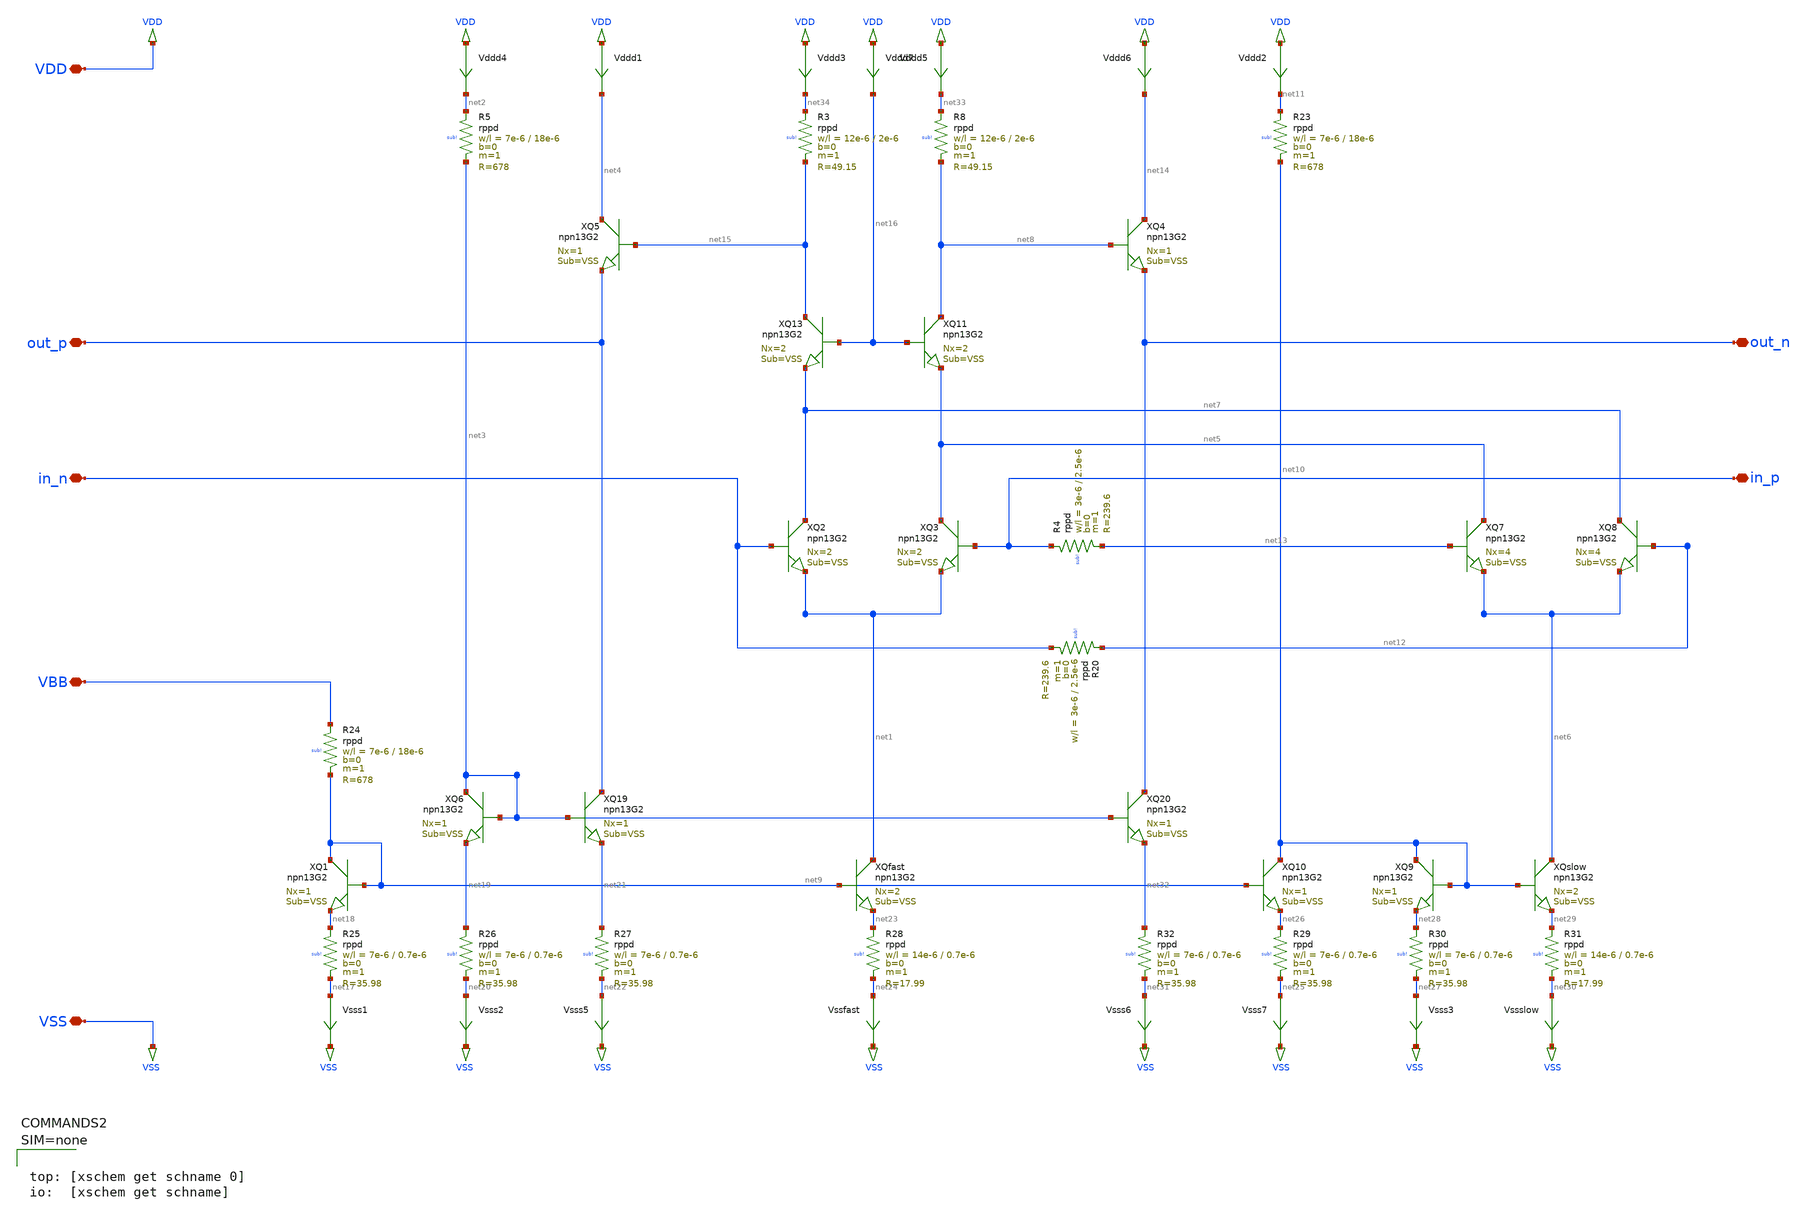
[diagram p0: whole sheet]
** sch_path: HBT_VCO_active_L/design_data/xschem/VCO_HBT_inv_dual_dly.sch
* Copyright (C) 1998-2023 Stefan Frederik Schippers
* This program is free software; you can redistribute it and/or modify
* it under the terms of the GNU General Public License as published by
* the Free Software Foundation; either version 2 of the License, or
* (at your option) any later version.
* This program is distributed in the hope that it will be useful,
* but WITHOUT ANY WARRANTY; without even the implied warranty of
* MERCHANTABILITY or FITNESS FOR A PARTICULAR PURPOSE.  See the
* GNU General Public License for more details.
* You should have received a copy of the GNU General Public License
* along with this program; if not, write to the Free Software
**.subckt VCO_HBT_inv_dual_dly VSS VBB out_p out_n VDD in_n in_p
*.iopin VSS
*.iopin VBB
*.iopin out_p
*.iopin out_n
*.iopin VDD
*.iopin in_n
*.iopin in_p
Vssfast net24 VSS 0
.save i(vssfast)
XQfast net1 net9 net23 VSS npn13G2 Nx=2
Vsss5 net22 VSS 0
.save i(vsss5)
XQ19 out_p net3 net21 VSS npn13G2 Nx=1
Vsss6 net31 VSS 0
.save i(vsss6)
XQ20 out_n net3 net32 VSS npn13G2 Nx=1
XQ2 net7 in_n net1 VSS npn13G2 Nx=2
XQ3 net5 in_p net1 VSS npn13G2 Nx=2
XQ4 net14 net8 out_n VSS npn13G2 Nx=1
XQ5 net4 net15 out_p VSS npn13G2 Nx=1
Vsss2 net20 VSS 0
.save i(vsss2)
XQ6 net3 net3 net19 VSS npn13G2 Nx=1
Vddd4 VDD net2 0
.save i(vddd4)
Vddd3 VDD net34 0
.save i(vddd3)
Vddd1 VDD net4 0
.save i(vddd1)
Vddd5 VDD net33 0
.save i(vddd5)
Vddd6 VDD net14 0
.save i(vddd6)
Vssslow net30 VSS 0
.save i(vssslow)
XQslow net6 net10 net29 VSS npn13G2 Nx=2
XQ7 net5 net13 net6 VSS npn13G2 Nx=4
XQ8 net7 net12 net6 VSS npn13G2 Nx=4
Vsss3 net27 VSS 0
.save i(vsss3)
XQ9 net10 net10 net28 VSS npn13G2 Nx=1
Vsss7 net25 VSS 0
.save i(vsss7)
XQ10 net10 net9 net26 VSS npn13G2 Nx=1
Vddd2 VDD net11 0
.save i(vddd2)
XQ11 net8 net16 net5 VSS npn13G2 Nx=2
XQ13 net15 net16 net7 VSS npn13G2 Nx=2
Vddd7 VDD net16 0
.save i(vddd7)
XR3 net34 net15 sub! rppd w=12e-6 l=2e-6 m=1 b=0 mm_ok=1
XR20 net12 in_n sub! rppd w=3e-6 l=2.5e-6 m=1 b=0 mm_ok=1
XR4 in_p net13 sub! rppd w=3e-6 l=2.5e-6 m=1 b=0 mm_ok=1
XR5 net2 net3 sub! rppd w=7e-6 l=18e-6 m=1 b=0 mm_ok=1
Vsss1 net17 VSS 0
.save i(vsss1)
XQ1 net9 net9 net18 VSS npn13G2 Nx=1
XR24 VBB net9 sub! rppd w=7e-6 l=18e-6 m=1 b=0 mm_ok=1
XR25 net18 net17 sub! rppd w=7e-6 l=0.7e-6 m=1 b=0 mm_ok=1
XR26 net19 net20 sub! rppd w=7e-6 l=0.7e-6 m=1 b=0 mm_ok=1
XR27 net21 net22 sub! rppd w=7e-6 l=0.7e-6 m=1 b=0 mm_ok=1
XR28 net23 net24 sub! rppd w=14e-6 l=0.7e-6 m=1 b=0 mm_ok=1
XR29 net26 net25 sub! rppd w=7e-6 l=0.7e-6 m=1 b=0 mm_ok=1
XR30 net28 net27 sub! rppd w=7e-6 l=0.7e-6 m=1 b=0 mm_ok=1
XR31 net29 net30 sub! rppd w=14e-6 l=0.7e-6 m=1 b=0 mm_ok=1
XR32 net32 net31 sub! rppd w=7e-6 l=0.7e-6 m=1 b=0 mm_ok=1
XR23 net11 net10 sub! rppd w=7e-6 l=18e-6 m=1 b=0 mm_ok=1
XR8 net33 net8 sub! rppd w=12e-6 l=2e-6 m=1 b=0 mm_ok=1
**** begin user architecture code



**** end user architecture code
**.ends
.end
